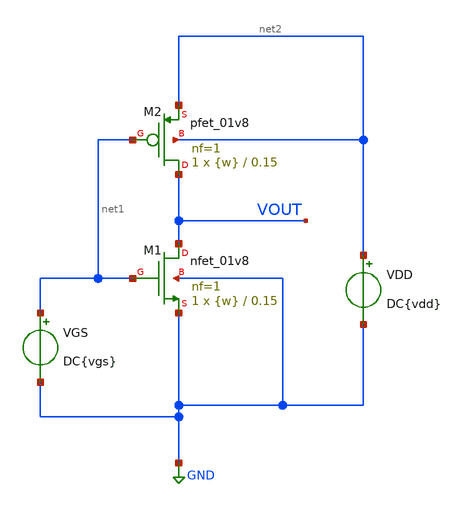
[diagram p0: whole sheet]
** sch_path: tp2/tp1_1.sch
**.subckt tp1_1
XM1 VOUT net1 GND GND sky130_fd_pr__nfet_01v8 L=0.15 W={w} nf=1 ad='int((nf+1)/2) * W/nf * 0.29' as='int((nf+2)/2) * W/nf * 0.29'
+ pd='2*int((nf+1)/2) * (W/nf + 0.29)' ps='2*int((nf+2)/2) * (W/nf + 0.29)' nrd='0.29 / W' nrs='0.29 / W'
+ sa=0 sb=0 sd=0 mult=1 m=1
VGS net1 GND DC{vgs}
VDD net2 GND DC{vdd}
XM2 VOUT net1 net2 net2 sky130_fd_pr__pfet_01v8 L=0.15 W={w} nf=1 ad='int((nf+1)/2) * W/nf * 0.29' as='int((nf+2)/2) * W/nf * 0.29'
+ pd='2*int((nf+1)/2) * (W/nf + 0.29)' ps='2*int((nf+2)/2) * (W/nf + 0.29)' nrd='0.29 / W' nrs='0.29 / W'
+ sa=0 sb=0 sd=0 mult=1 m=1
**** begin user architecture code



* Parameters
.param vdd = 1.8
.param vgs = 0.9
.param w=0.45
.options TEMP = -20



* Models
.lib ~/skywater/skywater-pdk/libraries/sky130_fd_pr_ngspice/latest/models/corners/sky130.lib TT

* Data to save
.save all  @M.XM1.msky130_fd_pr__nfet_01v8[id]  @M.XM1.msky130_fd_pr__nfet_01v8[value]  @M.XM1.msky130_fd_pr__nfet_01v8[gm]  @M.XM1.msky130_fd_pr__nfet_01v8[vth]  @M.XM1.msky130_fd_pr__nfet_01v8[vds]  @M.XM1.msky130_fd_pr__nfet_01v8[vdsat]  @M.XM1.msky130_fd_pr__nfet_01v8[vgs]  @M.XM2.msky130_fd_pr__pfet_01v8[id]  @M.XM2.msky130_fd_pr__pfet_01v8[gm]  @M.XM2.msky130_fd_pr__pfet_01v8[vth]  @M.XM2.msky130_fd_pr__pfet_01v8[vsd]  @M.XM2.msky130_fd_pr__pfet_01v8[vdsat]  @M.XM2.msky130_fd_pr__pfet_01v8[vsg]

* Simulation
.control

  let i = 0.75
  let n = 1.0

  while i <= n
   alter w = i
   reset
   dc VGS 0 2.3 0.01dc VGS 0.0 2.3 0.01
   let i=i+0.1
  end

  alterparam w = 0.45
  reset
  dc VGS 0 2.3 0.01

  alterparam w = 0.65
  reset
  dc VGS 0.0 2.3 0.01

  alterparam w = 0.75
  reset
  dc VGS 0.0 2.3 0.01

  plot @M.XM1.msky130_fd_pr__nfet_01v8[vds]
  set filetype = ascii
  write tp1_1_dc1.raw

.endc

.end


**** end user architecture code
**.ends
.GLOBAL GND
.end
